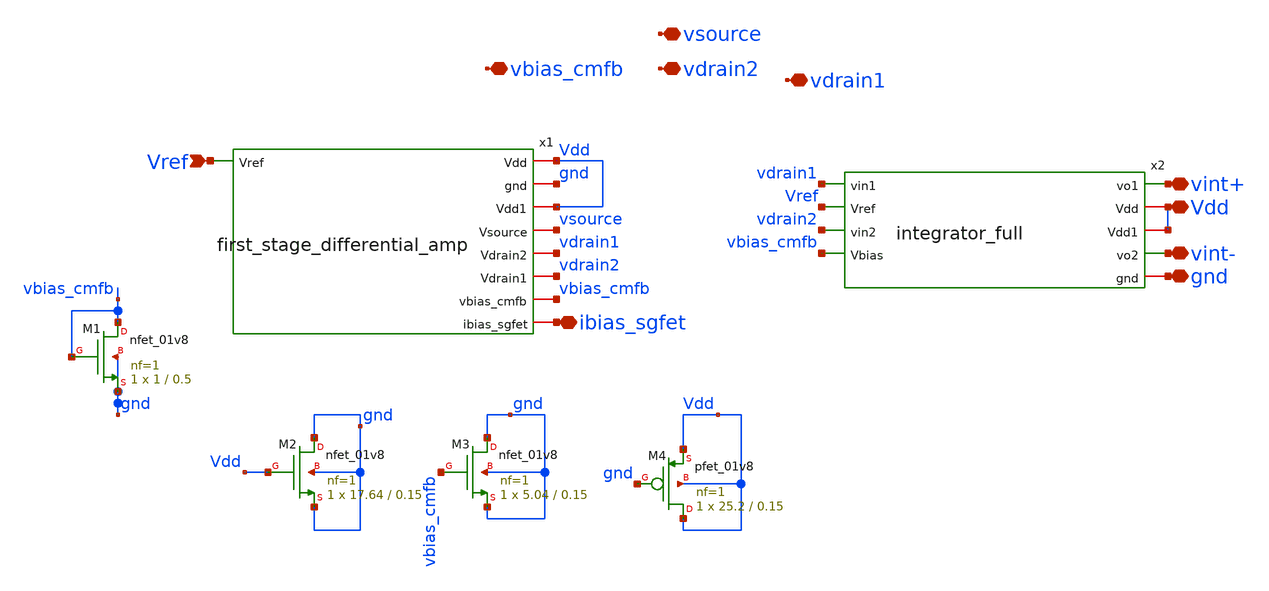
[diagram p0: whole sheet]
** sch_path: xschem/charge_pumps2/open_loop.sch
**.subckt open_loop gnd Vdd Vref vbias_cmfb vint+ vint- ibias_sgfet vsource vdrain2 vdrain1
*.iopin gnd
*.iopin Vdd
*.ipin Vref
*.iopin vbias_cmfb
*.iopin vint+
*.iopin vint-
*.iopin ibias_sgfet
*.iopin vsource
*.iopin vdrain2
*.iopin vdrain1
x1 Vdd gnd Vdd vsource vdrain1 vdrain2 Vref vbias_cmfb ibias_sgfet first_stage_differential_amp
x2 vint+ Vdd Vdd vint- gnd vdrain1 Vref vdrain2 vbias_cmfb integrator_full
XM1 vbias_cmfb vbias_cmfb gnd gnd sky130_fd_pr__nfet_01v8 L=0.5 W=1 nf=1 ad='int((nf+1)/2) * W/nf * 0.29'
+ as='int((nf+2)/2) * W/nf * 0.29' pd='2*int((nf+1)/2) * (W/nf + 0.29)' ps='2*int((nf+2)/2) * (W/nf + 0.29)'
+ nrd='0.29 / W' nrs='0.29 / W' sa=0 sb=0 sd=0 mult=1 m=1
XM2 gnd Vdd gnd gnd sky130_fd_pr__nfet_01v8 L=0.15 W=17.64 nf=1 ad='int((nf+1)/2) * W/nf * 0.29' as='int((nf+2)/2) * W/nf * 0.29'
+ pd='2*int((nf+1)/2) * (W/nf + 0.29)' ps='2*int((nf+2)/2) * (W/nf + 0.29)' nrd='0.29 / W' nrs='0.29 / W'
+ sa=0 sb=0 sd=0 mult=1 m=1
XM3 gnd vbias_cmfb gnd gnd sky130_fd_pr__nfet_01v8 L=0.15 W=5.04 nf=1 ad='int((nf+1)/2) * W/nf * 0.29'
+ as='int((nf+2)/2) * W/nf * 0.29' pd='2*int((nf+1)/2) * (W/nf + 0.29)' ps='2*int((nf+2)/2) * (W/nf + 0.29)'
+ nrd='0.29 / W' nrs='0.29 / W' sa=0 sb=0 sd=0 mult=1 m=1
XM4 Vdd gnd Vdd Vdd sky130_fd_pr__pfet_01v8 L=0.15 W=25.2 nf=1 ad='int((nf+1)/2) * W/nf * 0.29' as='int((nf+2)/2) * W/nf * 0.29'
+ pd='2*int((nf+1)/2) * (W/nf + 0.29)' ps='2*int((nf+2)/2) * (W/nf + 0.29)' nrd='0.29 / W' nrs='0.29 / W'
+ sa=0 sb=0 sd=0 mult=1 m=1
**.ends
.end
